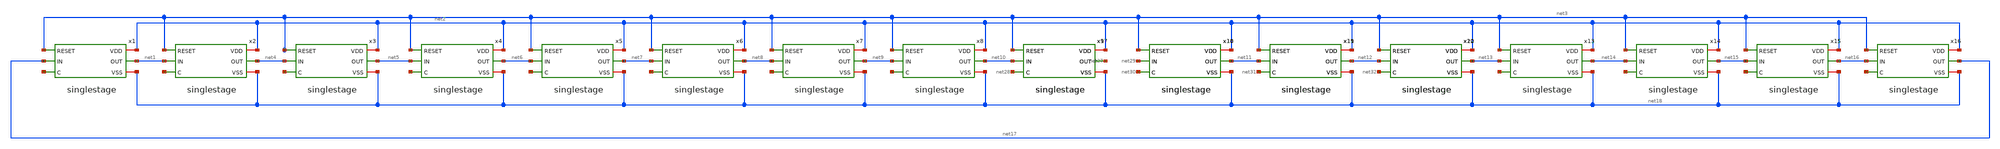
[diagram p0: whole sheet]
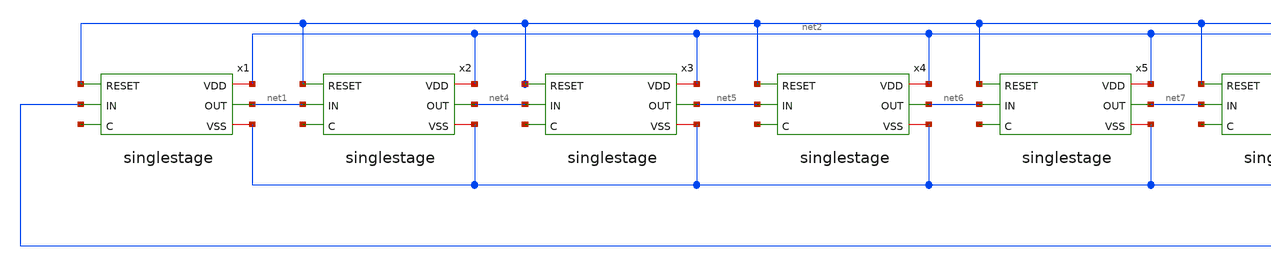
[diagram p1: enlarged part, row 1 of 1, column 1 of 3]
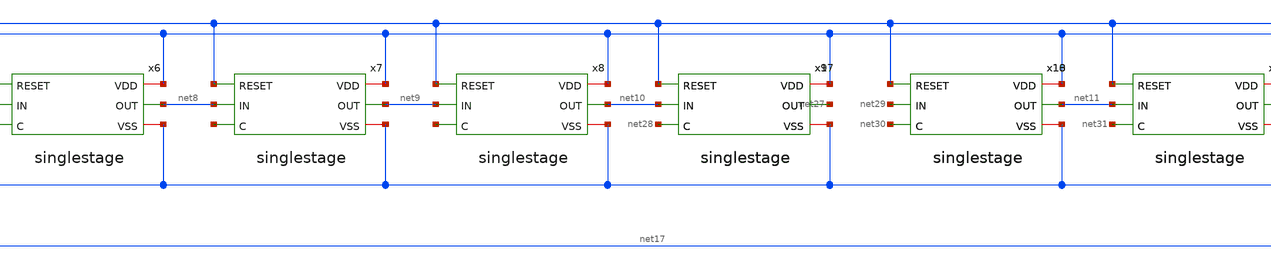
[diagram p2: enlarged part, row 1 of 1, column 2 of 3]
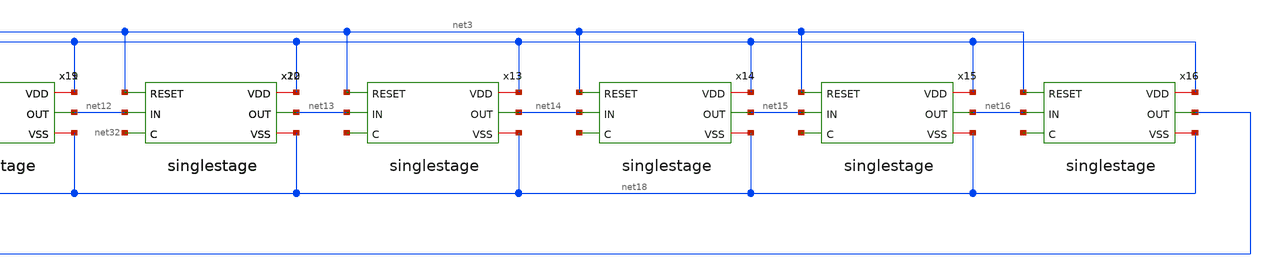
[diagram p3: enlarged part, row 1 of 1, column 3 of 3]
** sch_path: xiaolin/untitled.sch
**.subckt untitled
x1 net3 net2 net18 net1 net17 net19 singlestage
x2 net3 net2 net18 net4 net1 net20 singlestage
x3 net3 net2 net18 net5 net4 net21 singlestage
x4 net3 net2 net18 net6 net5 net22 singlestage
x5 net3 net2 net18 net7 net6 net23 singlestage
x6 net3 net2 net18 net8 net7 net24 singlestage
x7 net3 net2 net18 net9 net8 net25 singlestage
x8 net3 net2 net18 net10 net9 net26 singlestage
x9 net3 net2 net18 net27 net10 net28 singlestage
x10 net3 net2 net18 net11 net29 net30 singlestage
x11 net3 net2 net18 net12 net11 net31 singlestage
x12 net3 net2 net18 net13 net12 net32 singlestage
x13 net3 net2 net18 net14 net13 net33 singlestage
x14 net3 net2 net18 net15 net14 net34 singlestage
x15 net3 net2 net18 net16 net15 net35 singlestage
x16 net3 net2 net18 net17 net16 net36 singlestage
x17 net3 net2 net18 net27 net10 net28 singlestage
x18 net3 net2 net18 net11 net29 net30 singlestage
x19 net3 net2 net18 net12 net11 net31 singlestage
x20 net3 net2 net18 net13 net12 net32 singlestage
**.ends

* expanding   symbol:  singlestage.sym # of pins=6
** sym_path: design/singlestage.sym
** sch_path: design/singlestage.sch
.subckt singlestage RESET VDD VSS OUT IN C
*.ipin IN
*.ipin C
*.ipin RESET
*.iopin VSS
*.iopin VDD
*.opin OUT
x1 RESET net1 VSS VSS VDD VDD net3 sky130_fd_sc_hd__nor2_1
x2 RESET net2 VSS VSS VDD VDD net4 sky130_fd_sc_hd__nor2_1
x3 net6 VSS net1 VDD IN net5 net2 demux2-1
x4 net6 VSS net3 VDD OUT net5 net4 mux2-1
x5 net5 VSS VSS VDD VDD net6 sky130_fd_sc_hd__inv_1
XM1 net1 net6 VDD VDD sky130_fd_pr__pfet_01v8_hvt L=0.15 W=1 nf=1 ad='int((nf+1)/2) * W/nf * 0.29' as='int((nf+2)/2) * W/nf * 0.29'
+ pd='2*int((nf+1)/2) * (W/nf + 0.29)' ps='2*int((nf+2)/2) * (W/nf + 0.29)' nrd='0.29 / W' nrs='0.29 / W'
+ sa=0 sb=0 sd=0 mult=1 m=1
XM2 net2 net5 VDD VDD sky130_fd_pr__pfet_01v8_hvt L=0.15 W=1 nf=1 ad='int((nf+1)/2) * W/nf * 0.29' as='int((nf+2)/2) * W/nf * 0.29'
+ pd='2*int((nf+1)/2) * (W/nf + 0.29)' ps='2*int((nf+2)/2) * (W/nf + 0.29)' nrd='0.29 / W' nrs='0.29 / W'
+ sa=0 sb=0 sd=0 mult=1 m=1
x6 C VSS VSS VDD VDD net5 sky130_fd_sc_hd__inv_1
.ends


* expanding   symbol:  demux2-1.sym # of pins=7
** sym_path: xiaolin/demux2-1.sym
** sch_path: xiaolin/demux2-1.sch
.subckt demux2-1 S VSS OUT1 VDD IN Sbar OUT2
*.ipin Sbar
*.ipin S
*.iopin VSS
*.iopin VDD
*.opin OUT1
*.opin OUT2
*.ipin IN
XM2 IN S OUT1 VSS sky130_fd_pr__nfet_01v8 L=0.15 W=0.65 nf=1 ad='int((nf+1)/2) * W/nf * 0.29' as='int((nf+2)/2) * W/nf * 0.29'
+ pd='2*int((nf+1)/2) * (W/nf + 0.29)' ps='2*int((nf+2)/2) * (W/nf + 0.29)' nrd='0.29 / W' nrs='0.29 / W'
+ sa=0 sb=0 sd=0 mult=1 m=1
XM1 IN Sbar OUT2 VSS sky130_fd_pr__nfet_01v8 L=0.15 W=0.65 nf=1 ad='int((nf+1)/2) * W/nf * 0.29' as='int((nf+2)/2) * W/nf * 0.29'
+ pd='2*int((nf+1)/2) * (W/nf + 0.29)' ps='2*int((nf+2)/2) * (W/nf + 0.29)' nrd='0.29 / W' nrs='0.29 / W'
+ sa=0 sb=0 sd=0 mult=1 m=1
XM3 IN S OUT2 VDD sky130_fd_pr__pfet_01v8_hvt L=0.15 W=1 nf=1 ad='int((nf+1)/2) * W/nf * 0.29' as='int((nf+2)/2) * W/nf * 0.29'
+ pd='2*int((nf+1)/2) * (W/nf + 0.29)' ps='2*int((nf+2)/2) * (W/nf + 0.29)' nrd='0.29 / W' nrs='0.29 / W'
+ sa=0 sb=0 sd=0 mult=1 m=1
XM4 IN Sbar OUT1 VDD sky130_fd_pr__pfet_01v8_hvt L=0.15 W=1 nf=1 ad='int((nf+1)/2) * W/nf * 0.29' as='int((nf+2)/2) * W/nf * 0.29'
+ pd='2*int((nf+1)/2) * (W/nf + 0.29)' ps='2*int((nf+2)/2) * (W/nf + 0.29)' nrd='0.29 / W' nrs='0.29 / W'
+ sa=0 sb=0 sd=0 mult=1 m=1
XM5 IN S OUT2 VDD sky130_fd_pr__pfet_01v8_hvt L=0.15 W=1 nf=1 ad='int((nf+1)/2) * W/nf * 0.29' as='int((nf+2)/2) * W/nf * 0.29'
+ pd='2*int((nf+1)/2) * (W/nf + 0.29)' ps='2*int((nf+2)/2) * (W/nf + 0.29)' nrd='0.29 / W' nrs='0.29 / W'
+ sa=0 sb=0 sd=0 mult=1 m=1
.ends


* expanding   symbol:  mux2-1.sym # of pins=7
** sym_path: design/mux2-1.sym
** sch_path: design/mux2-1.sch
.subckt mux2-1 S VSS IN1 VDD OUT Sbar IN2
*.ipin IN1
*.ipin IN2
*.ipin Sbar
*.ipin S
*.opin OUT
*.iopin VSS
*.iopin VDD
XM2 IN1 S OUT VSS sky130_fd_pr__nfet_01v8 L=0.15 W=0.65 nf=1 ad='int((nf+1)/2) * W/nf * 0.29' as='int((nf+2)/2) * W/nf * 0.29'
+ pd='2*int((nf+1)/2) * (W/nf + 0.29)' ps='2*int((nf+2)/2) * (W/nf + 0.29)' nrd='0.29 / W' nrs='0.29 / W'
+ sa=0 sb=0 sd=0 mult=1 m=1
XM1 IN2 Sbar OUT VSS sky130_fd_pr__nfet_01v8 L=0.15 W=0.65 nf=1 ad='int((nf+1)/2) * W/nf * 0.29' as='int((nf+2)/2) * W/nf * 0.29'
+ pd='2*int((nf+1)/2) * (W/nf + 0.29)' ps='2*int((nf+2)/2) * (W/nf + 0.29)' nrd='0.29 / W' nrs='0.29 / W'
+ sa=0 sb=0 sd=0 mult=1 m=1
XM4 IN1 Sbar OUT VDD sky130_fd_pr__pfet_01v8_hvt L=0.15 W=1 nf=1 ad='int((nf+1)/2) * W/nf * 0.29' as='int((nf+2)/2) * W/nf * 0.29'
+ pd='2*int((nf+1)/2) * (W/nf + 0.29)' ps='2*int((nf+2)/2) * (W/nf + 0.29)' nrd='0.29 / W' nrs='0.29 / W'
+ sa=0 sb=0 sd=0 mult=1 m=1
XM5 IN2 S OUT VDD sky130_fd_pr__pfet_01v8_hvt L=0.15 W=1 nf=1 ad='int((nf+1)/2) * W/nf * 0.29' as='int((nf+2)/2) * W/nf * 0.29'
+ pd='2*int((nf+1)/2) * (W/nf + 0.29)' ps='2*int((nf+2)/2) * (W/nf + 0.29)' nrd='0.29 / W' nrs='0.29 / W'
+ sa=0 sb=0 sd=0 mult=1 m=1
.ends

.end
